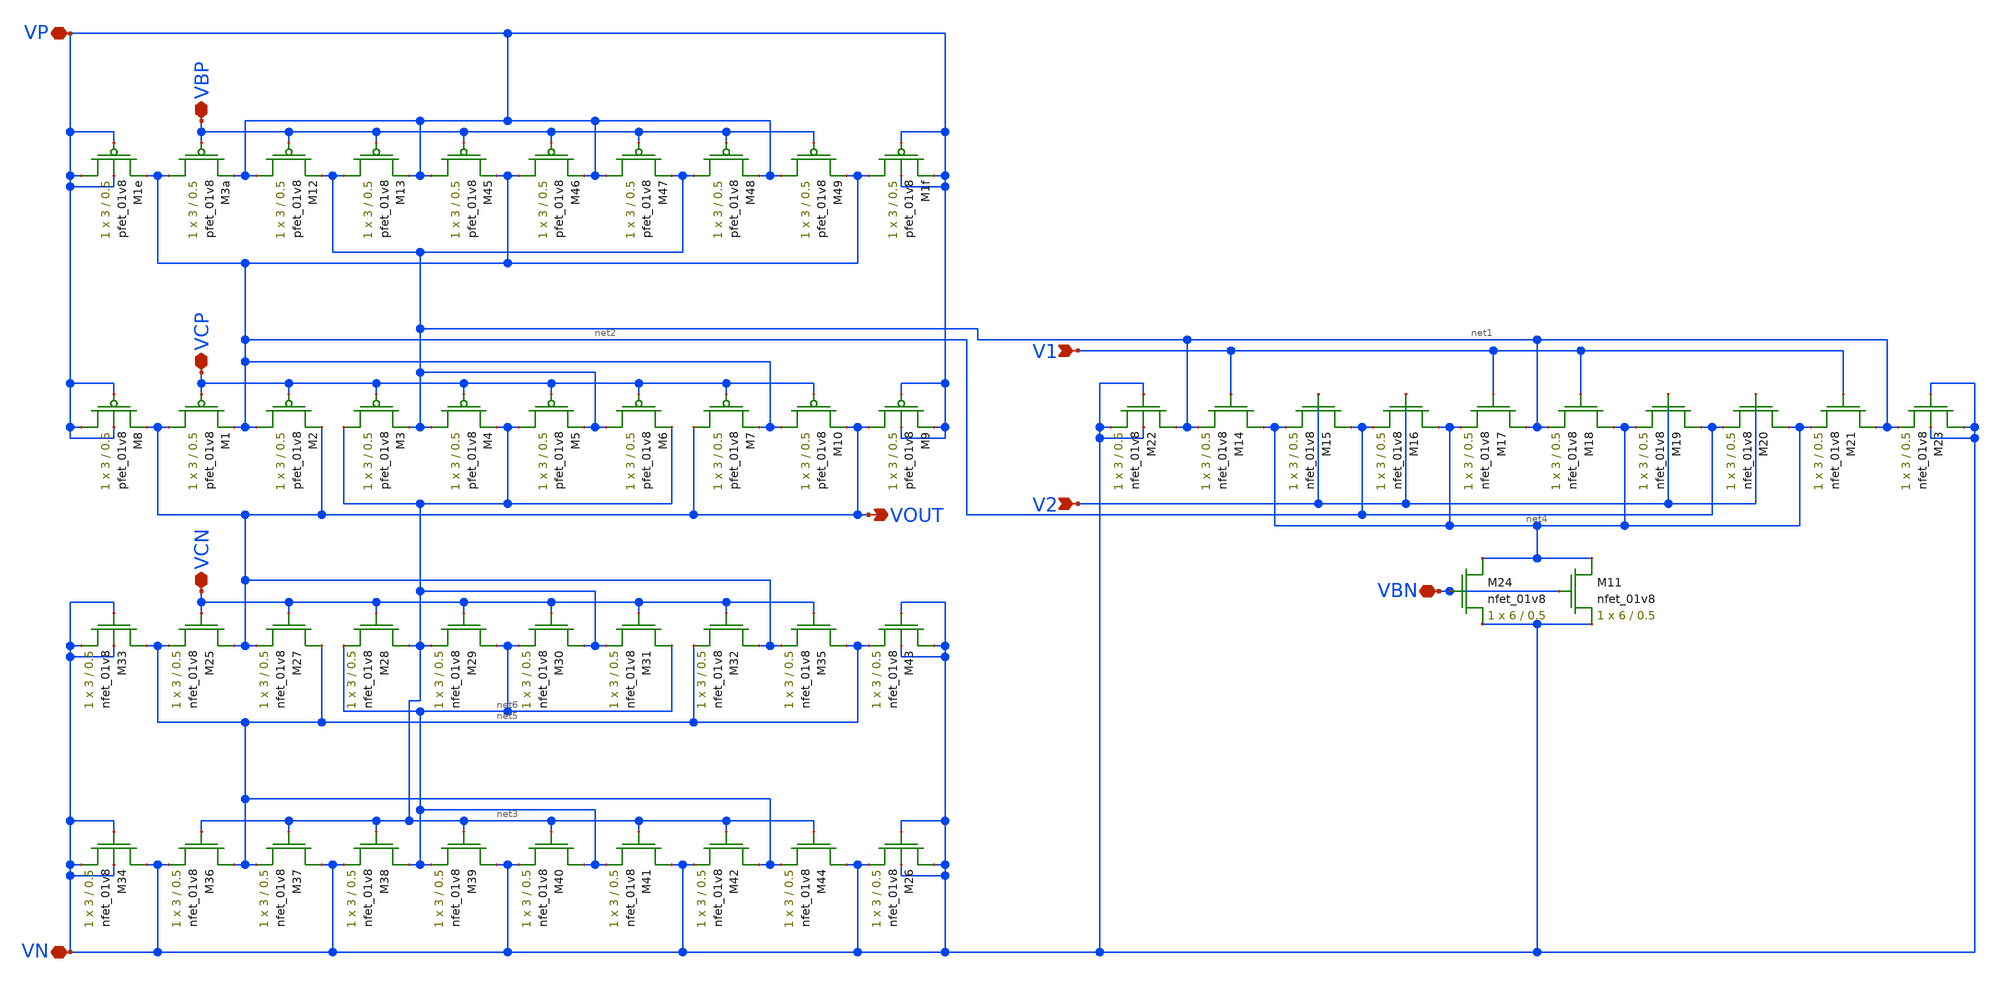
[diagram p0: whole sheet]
** sch_path: differential_amplifier/schematics/folded_cascode_differential_amplifier.sch
**.subckt folded_cascode_differential_amplifier VBP VCP V1 V2 VBN VCN VP VN VOUT
*.iopin VBP
*.iopin VCP
*.ipin V1
*.ipin V2
*.iopin VBN
*.iopin VCN
*.iopin VP
*.iopin VN
*.opin VOUT
XM3a net2 VBP VP VP sky130_fd_pr__pfet_01v8 L=0.5 W=3 nf=1 ad='int((nf+1)/2) * W/nf * 0.29' as='int((nf+2)/2) * W/nf * 0.29'
+ pd='2*int((nf+1)/2) * (W/nf + 0.29)' ps='2*int((nf+2)/2) * (W/nf + 0.29)' nrd='0.29 / W' nrs='0.29 / W'
+ sa=0 sb=0 sd=0 mult=1 m=1
XM1e VP VP net2 VP sky130_fd_pr__pfet_01v8 L=0.5 W=3 nf=1 ad='int((nf+1)/2) * W/nf * 0.29' as='int((nf+2)/2) * W/nf * 0.29'
+ pd='2*int((nf+1)/2) * (W/nf + 0.29)' ps='2*int((nf+2)/2) * (W/nf + 0.29)' nrd='0.29 / W' nrs='0.29 / W'
+ sa=0 sb=0 sd=0 mult=1 m=1
XM1f net2 VP VP VP sky130_fd_pr__pfet_01v8 L=0.5 W=3 nf=1 ad='int((nf+1)/2) * W/nf * 0.29' as='int((nf+2)/2) * W/nf * 0.29'
+ pd='2*int((nf+1)/2) * (W/nf + 0.29)' ps='2*int((nf+2)/2) * (W/nf + 0.29)' nrd='0.29 / W' nrs='0.29 / W'
+ sa=0 sb=0 sd=0 mult=1 m=1
XM8 VP VP VOUT VP sky130_fd_pr__pfet_01v8 L=0.5 W=3 nf=1 ad='int((nf+1)/2) * W/nf * 0.29' as='int((nf+2)/2) * W/nf * 0.29'
+ pd='2*int((nf+1)/2) * (W/nf + 0.29)' ps='2*int((nf+2)/2) * (W/nf + 0.29)' nrd='0.29 / W' nrs='0.29 / W'
+ sa=0 sb=0 sd=0 mult=1 m=1
XM9 VOUT VP VP VP sky130_fd_pr__pfet_01v8 L=0.5 W=3 nf=1 ad='int((nf+1)/2) * W/nf * 0.29' as='int((nf+2)/2) * W/nf * 0.29'
+ pd='2*int((nf+1)/2) * (W/nf + 0.29)' ps='2*int((nf+2)/2) * (W/nf + 0.29)' nrd='0.29 / W' nrs='0.29 / W'
+ sa=0 sb=0 sd=0 mult=1 m=1
XM22 net1 VN VN VN sky130_fd_pr__nfet_01v8 L=0.5 W=3 nf=1 ad='int((nf+1)/2) * W/nf * 0.29' as='int((nf+2)/2) * W/nf * 0.29'
+ pd='2*int((nf+1)/2) * (W/nf + 0.29)' ps='2*int((nf+2)/2) * (W/nf + 0.29)' nrd='0.29 / W' nrs='0.29 / W'
+ sa=0 sb=0 sd=0 mult=1 m=1
XM23 VN VN net1 VN sky130_fd_pr__nfet_01v8 L=0.5 W=3 nf=1 ad='int((nf+1)/2) * W/nf * 0.29' as='int((nf+2)/2) * W/nf * 0.29'
+ pd='2*int((nf+1)/2) * (W/nf + 0.29)' ps='2*int((nf+2)/2) * (W/nf + 0.29)' nrd='0.29 / W' nrs='0.29 / W'
+ sa=0 sb=0 sd=0 mult=1 m=1
XM24 net4 VBN VN VN sky130_fd_pr__nfet_01v8 L=0.5 W=6 nf=1 ad='int((nf+1)/2) * W/nf * 0.29' as='int((nf+2)/2) * W/nf * 0.29'
+ pd='2*int((nf+1)/2) * (W/nf + 0.29)' ps='2*int((nf+2)/2) * (W/nf + 0.29)' nrd='0.29 / W' nrs='0.29 / W'
+ sa=0 sb=0 sd=0 mult=1 m=1
XM25 VOUT VCN net5 VN sky130_fd_pr__nfet_01v8 L=0.5 W=3 nf=1 ad='int((nf+1)/2) * W/nf * 0.29' as='int((nf+2)/2) * W/nf * 0.29'
+ pd='2*int((nf+1)/2) * (W/nf + 0.29)' ps='2*int((nf+2)/2) * (W/nf + 0.29)' nrd='0.29 / W' nrs='0.29 / W'
+ sa=0 sb=0 sd=0 mult=1 m=1
XM33 net5 VN VN VN sky130_fd_pr__nfet_01v8 L=0.5 W=3 nf=1 ad='int((nf+1)/2) * W/nf * 0.29' as='int((nf+2)/2) * W/nf * 0.29'
+ pd='2*int((nf+1)/2) * (W/nf + 0.29)' ps='2*int((nf+2)/2) * (W/nf + 0.29)' nrd='0.29 / W' nrs='0.29 / W'
+ sa=0 sb=0 sd=0 mult=1 m=1
XM34 VN VN VN VN sky130_fd_pr__nfet_01v8 L=0.5 W=3 nf=1 ad='int((nf+1)/2) * W/nf * 0.29' as='int((nf+2)/2) * W/nf * 0.29'
+ pd='2*int((nf+1)/2) * (W/nf + 0.29)' ps='2*int((nf+2)/2) * (W/nf + 0.29)' nrd='0.29 / W' nrs='0.29 / W'
+ sa=0 sb=0 sd=0 mult=1 m=1
XM43 VN VN net5 VN sky130_fd_pr__nfet_01v8 L=0.5 W=3 nf=1 ad='int((nf+1)/2) * W/nf * 0.29' as='int((nf+2)/2) * W/nf * 0.29'
+ pd='2*int((nf+1)/2) * (W/nf + 0.29)' ps='2*int((nf+2)/2) * (W/nf + 0.29)' nrd='0.29 / W' nrs='0.29 / W'
+ sa=0 sb=0 sd=0 mult=1 m=1
XM11 net4 VBN VN VN sky130_fd_pr__nfet_01v8 L=0.5 W=6 nf=1 ad='int((nf+1)/2) * W/nf * 0.29' as='int((nf+2)/2) * W/nf * 0.29'
+ pd='2*int((nf+1)/2) * (W/nf + 0.29)' ps='2*int((nf+2)/2) * (W/nf + 0.29)' nrd='0.29 / W' nrs='0.29 / W'
+ sa=0 sb=0 sd=0 mult=1 m=1
XM12 VP VBP net1 VP sky130_fd_pr__pfet_01v8 L=0.5 W=3 nf=1 ad='int((nf+1)/2) * W/nf * 0.29' as='int((nf+2)/2) * W/nf * 0.29'
+ pd='2*int((nf+1)/2) * (W/nf + 0.29)' ps='2*int((nf+2)/2) * (W/nf + 0.29)' nrd='0.29 / W' nrs='0.29 / W'
+ sa=0 sb=0 sd=0 mult=1 m=1
XM13 net1 VBP VP VP sky130_fd_pr__pfet_01v8 L=0.5 W=3 nf=1 ad='int((nf+1)/2) * W/nf * 0.29' as='int((nf+2)/2) * W/nf * 0.29'
+ pd='2*int((nf+1)/2) * (W/nf + 0.29)' ps='2*int((nf+2)/2) * (W/nf + 0.29)' nrd='0.29 / W' nrs='0.29 / W'
+ sa=0 sb=0 sd=0 mult=1 m=1
XM45 VP VBP net2 VP sky130_fd_pr__pfet_01v8 L=0.5 W=3 nf=1 ad='int((nf+1)/2) * W/nf * 0.29' as='int((nf+2)/2) * W/nf * 0.29'
+ pd='2*int((nf+1)/2) * (W/nf + 0.29)' ps='2*int((nf+2)/2) * (W/nf + 0.29)' nrd='0.29 / W' nrs='0.29 / W'
+ sa=0 sb=0 sd=0 mult=1 m=1
XM46 net2 VBP VP VP sky130_fd_pr__pfet_01v8 L=0.5 W=3 nf=1 ad='int((nf+1)/2) * W/nf * 0.29' as='int((nf+2)/2) * W/nf * 0.29'
+ pd='2*int((nf+1)/2) * (W/nf + 0.29)' ps='2*int((nf+2)/2) * (W/nf + 0.29)' nrd='0.29 / W' nrs='0.29 / W'
+ sa=0 sb=0 sd=0 mult=1 m=1
XM47 VP VBP net1 VP sky130_fd_pr__pfet_01v8 L=0.5 W=3 nf=1 ad='int((nf+1)/2) * W/nf * 0.29' as='int((nf+2)/2) * W/nf * 0.29'
+ pd='2*int((nf+1)/2) * (W/nf + 0.29)' ps='2*int((nf+2)/2) * (W/nf + 0.29)' nrd='0.29 / W' nrs='0.29 / W'
+ sa=0 sb=0 sd=0 mult=1 m=1
XM48 net1 VBP VP VP sky130_fd_pr__pfet_01v8 L=0.5 W=3 nf=1 ad='int((nf+1)/2) * W/nf * 0.29' as='int((nf+2)/2) * W/nf * 0.29'
+ pd='2*int((nf+1)/2) * (W/nf + 0.29)' ps='2*int((nf+2)/2) * (W/nf + 0.29)' nrd='0.29 / W' nrs='0.29 / W'
+ sa=0 sb=0 sd=0 mult=1 m=1
XM49 VP VBP net2 VP sky130_fd_pr__pfet_01v8 L=0.5 W=3 nf=1 ad='int((nf+1)/2) * W/nf * 0.29' as='int((nf+2)/2) * W/nf * 0.29'
+ pd='2*int((nf+1)/2) * (W/nf + 0.29)' ps='2*int((nf+2)/2) * (W/nf + 0.29)' nrd='0.29 / W' nrs='0.29 / W'
+ sa=0 sb=0 sd=0 mult=1 m=1
XM1 VOUT VCP net2 VP sky130_fd_pr__pfet_01v8 L=0.5 W=3 nf=1 ad='int((nf+1)/2) * W/nf * 0.29' as='int((nf+2)/2) * W/nf * 0.29'
+ pd='2*int((nf+1)/2) * (W/nf + 0.29)' ps='2*int((nf+2)/2) * (W/nf + 0.29)' nrd='0.29 / W' nrs='0.29 / W'
+ sa=0 sb=0 sd=0 mult=1 m=1
XM2 net2 VCP VOUT VP sky130_fd_pr__pfet_01v8 L=0.5 W=3 nf=1 ad='int((nf+1)/2) * W/nf * 0.29' as='int((nf+2)/2) * W/nf * 0.29'
+ pd='2*int((nf+1)/2) * (W/nf + 0.29)' ps='2*int((nf+2)/2) * (W/nf + 0.29)' nrd='0.29 / W' nrs='0.29 / W'
+ sa=0 sb=0 sd=0 mult=1 m=1
XM3 net3 VCP net1 VP sky130_fd_pr__pfet_01v8 L=0.5 W=3 nf=1 ad='int((nf+1)/2) * W/nf * 0.29' as='int((nf+2)/2) * W/nf * 0.29'
+ pd='2*int((nf+1)/2) * (W/nf + 0.29)' ps='2*int((nf+2)/2) * (W/nf + 0.29)' nrd='0.29 / W' nrs='0.29 / W'
+ sa=0 sb=0 sd=0 mult=1 m=1
XM4 net1 VCP net3 VP sky130_fd_pr__pfet_01v8 L=0.5 W=3 nf=1 ad='int((nf+1)/2) * W/nf * 0.29' as='int((nf+2)/2) * W/nf * 0.29'
+ pd='2*int((nf+1)/2) * (W/nf + 0.29)' ps='2*int((nf+2)/2) * (W/nf + 0.29)' nrd='0.29 / W' nrs='0.29 / W'
+ sa=0 sb=0 sd=0 mult=1 m=1
XM5 net3 VCP net1 VP sky130_fd_pr__pfet_01v8 L=0.5 W=3 nf=1 ad='int((nf+1)/2) * W/nf * 0.29' as='int((nf+2)/2) * W/nf * 0.29'
+ pd='2*int((nf+1)/2) * (W/nf + 0.29)' ps='2*int((nf+2)/2) * (W/nf + 0.29)' nrd='0.29 / W' nrs='0.29 / W'
+ sa=0 sb=0 sd=0 mult=1 m=1
XM6 net1 VCP net3 VP sky130_fd_pr__pfet_01v8 L=0.5 W=3 nf=1 ad='int((nf+1)/2) * W/nf * 0.29' as='int((nf+2)/2) * W/nf * 0.29'
+ pd='2*int((nf+1)/2) * (W/nf + 0.29)' ps='2*int((nf+2)/2) * (W/nf + 0.29)' nrd='0.29 / W' nrs='0.29 / W'
+ sa=0 sb=0 sd=0 mult=1 m=1
XM7 VOUT VCP net2 VP sky130_fd_pr__pfet_01v8 L=0.5 W=3 nf=1 ad='int((nf+1)/2) * W/nf * 0.29' as='int((nf+2)/2) * W/nf * 0.29'
+ pd='2*int((nf+1)/2) * (W/nf + 0.29)' ps='2*int((nf+2)/2) * (W/nf + 0.29)' nrd='0.29 / W' nrs='0.29 / W'
+ sa=0 sb=0 sd=0 mult=1 m=1
XM10 net2 VCP VOUT VP sky130_fd_pr__pfet_01v8 L=0.5 W=3 nf=1 ad='int((nf+1)/2) * W/nf * 0.29' as='int((nf+2)/2) * W/nf * 0.29'
+ pd='2*int((nf+1)/2) * (W/nf + 0.29)' ps='2*int((nf+2)/2) * (W/nf + 0.29)' nrd='0.29 / W' nrs='0.29 / W'
+ sa=0 sb=0 sd=0 mult=1 m=1
XM26 VN VN VN VN sky130_fd_pr__nfet_01v8 L=0.5 W=3 nf=1 ad='int((nf+1)/2) * W/nf * 0.29' as='int((nf+2)/2) * W/nf * 0.29'
+ pd='2*int((nf+1)/2) * (W/nf + 0.29)' ps='2*int((nf+2)/2) * (W/nf + 0.29)' nrd='0.29 / W' nrs='0.29 / W'
+ sa=0 sb=0 sd=0 mult=1 m=1
XM27 net5 VCN VOUT VN sky130_fd_pr__nfet_01v8 L=0.5 W=3 nf=1 ad='int((nf+1)/2) * W/nf * 0.29' as='int((nf+2)/2) * W/nf * 0.29'
+ pd='2*int((nf+1)/2) * (W/nf + 0.29)' ps='2*int((nf+2)/2) * (W/nf + 0.29)' nrd='0.29 / W' nrs='0.29 / W'
+ sa=0 sb=0 sd=0 mult=1 m=1
XM28 net3 VCN net6 VN sky130_fd_pr__nfet_01v8 L=0.5 W=3 nf=1 ad='int((nf+1)/2) * W/nf * 0.29' as='int((nf+2)/2) * W/nf * 0.29'
+ pd='2*int((nf+1)/2) * (W/nf + 0.29)' ps='2*int((nf+2)/2) * (W/nf + 0.29)' nrd='0.29 / W' nrs='0.29 / W'
+ sa=0 sb=0 sd=0 mult=1 m=1
XM29 net6 VCN net3 VN sky130_fd_pr__nfet_01v8 L=0.5 W=3 nf=1 ad='int((nf+1)/2) * W/nf * 0.29' as='int((nf+2)/2) * W/nf * 0.29'
+ pd='2*int((nf+1)/2) * (W/nf + 0.29)' ps='2*int((nf+2)/2) * (W/nf + 0.29)' nrd='0.29 / W' nrs='0.29 / W'
+ sa=0 sb=0 sd=0 mult=1 m=1
XM30 net3 VCN net6 VN sky130_fd_pr__nfet_01v8 L=0.5 W=3 nf=1 ad='int((nf+1)/2) * W/nf * 0.29' as='int((nf+2)/2) * W/nf * 0.29'
+ pd='2*int((nf+1)/2) * (W/nf + 0.29)' ps='2*int((nf+2)/2) * (W/nf + 0.29)' nrd='0.29 / W' nrs='0.29 / W'
+ sa=0 sb=0 sd=0 mult=1 m=1
XM31 net6 VCN net3 VN sky130_fd_pr__nfet_01v8 L=0.5 W=3 nf=1 ad='int((nf+1)/2) * W/nf * 0.29' as='int((nf+2)/2) * W/nf * 0.29'
+ pd='2*int((nf+1)/2) * (W/nf + 0.29)' ps='2*int((nf+2)/2) * (W/nf + 0.29)' nrd='0.29 / W' nrs='0.29 / W'
+ sa=0 sb=0 sd=0 mult=1 m=1
XM32 VOUT VCN net5 VN sky130_fd_pr__nfet_01v8 L=0.5 W=3 nf=1 ad='int((nf+1)/2) * W/nf * 0.29' as='int((nf+2)/2) * W/nf * 0.29'
+ pd='2*int((nf+1)/2) * (W/nf + 0.29)' ps='2*int((nf+2)/2) * (W/nf + 0.29)' nrd='0.29 / W' nrs='0.29 / W'
+ sa=0 sb=0 sd=0 mult=1 m=1
XM35 net5 VCN VOUT VN sky130_fd_pr__nfet_01v8 L=0.5 W=3 nf=1 ad='int((nf+1)/2) * W/nf * 0.29' as='int((nf+2)/2) * W/nf * 0.29'
+ pd='2*int((nf+1)/2) * (W/nf + 0.29)' ps='2*int((nf+2)/2) * (W/nf + 0.29)' nrd='0.29 / W' nrs='0.29 / W'
+ sa=0 sb=0 sd=0 mult=1 m=1
XM36 net5 net3 VN VN sky130_fd_pr__nfet_01v8 L=0.5 W=3 nf=1 ad='int((nf+1)/2) * W/nf * 0.29' as='int((nf+2)/2) * W/nf * 0.29'
+ pd='2*int((nf+1)/2) * (W/nf + 0.29)' ps='2*int((nf+2)/2) * (W/nf + 0.29)' nrd='0.29 / W' nrs='0.29 / W'
+ sa=0 sb=0 sd=0 mult=1 m=1
XM37 VN net3 net5 VN sky130_fd_pr__nfet_01v8 L=0.5 W=3 nf=1 ad='int((nf+1)/2) * W/nf * 0.29' as='int((nf+2)/2) * W/nf * 0.29'
+ pd='2*int((nf+1)/2) * (W/nf + 0.29)' ps='2*int((nf+2)/2) * (W/nf + 0.29)' nrd='0.29 / W' nrs='0.29 / W'
+ sa=0 sb=0 sd=0 mult=1 m=1
XM38 net6 net3 VN VN sky130_fd_pr__nfet_01v8 L=0.5 W=3 nf=1 ad='int((nf+1)/2) * W/nf * 0.29' as='int((nf+2)/2) * W/nf * 0.29'
+ pd='2*int((nf+1)/2) * (W/nf + 0.29)' ps='2*int((nf+2)/2) * (W/nf + 0.29)' nrd='0.29 / W' nrs='0.29 / W'
+ sa=0 sb=0 sd=0 mult=1 m=1
XM39 VN net3 net6 VN sky130_fd_pr__nfet_01v8 L=0.5 W=3 nf=1 ad='int((nf+1)/2) * W/nf * 0.29' as='int((nf+2)/2) * W/nf * 0.29'
+ pd='2*int((nf+1)/2) * (W/nf + 0.29)' ps='2*int((nf+2)/2) * (W/nf + 0.29)' nrd='0.29 / W' nrs='0.29 / W'
+ sa=0 sb=0 sd=0 mult=1 m=1
XM40 net6 net3 VN VN sky130_fd_pr__nfet_01v8 L=0.5 W=3 nf=1 ad='int((nf+1)/2) * W/nf * 0.29' as='int((nf+2)/2) * W/nf * 0.29'
+ pd='2*int((nf+1)/2) * (W/nf + 0.29)' ps='2*int((nf+2)/2) * (W/nf + 0.29)' nrd='0.29 / W' nrs='0.29 / W'
+ sa=0 sb=0 sd=0 mult=1 m=1
XM41 VN net3 net6 VN sky130_fd_pr__nfet_01v8 L=0.5 W=3 nf=1 ad='int((nf+1)/2) * W/nf * 0.29' as='int((nf+2)/2) * W/nf * 0.29'
+ pd='2*int((nf+1)/2) * (W/nf + 0.29)' ps='2*int((nf+2)/2) * (W/nf + 0.29)' nrd='0.29 / W' nrs='0.29 / W'
+ sa=0 sb=0 sd=0 mult=1 m=1
XM42 net5 net3 VN VN sky130_fd_pr__nfet_01v8 L=0.5 W=3 nf=1 ad='int((nf+1)/2) * W/nf * 0.29' as='int((nf+2)/2) * W/nf * 0.29'
+ pd='2*int((nf+1)/2) * (W/nf + 0.29)' ps='2*int((nf+2)/2) * (W/nf + 0.29)' nrd='0.29 / W' nrs='0.29 / W'
+ sa=0 sb=0 sd=0 mult=1 m=1
XM44 VN net3 net5 VN sky130_fd_pr__nfet_01v8 L=0.5 W=3 nf=1 ad='int((nf+1)/2) * W/nf * 0.29' as='int((nf+2)/2) * W/nf * 0.29'
+ pd='2*int((nf+1)/2) * (W/nf + 0.29)' ps='2*int((nf+2)/2) * (W/nf + 0.29)' nrd='0.29 / W' nrs='0.29 / W'
+ sa=0 sb=0 sd=0 mult=1 m=1
XM14 net4 V1 net1 VN sky130_fd_pr__nfet_01v8 L=0.5 W=3 nf=1 ad='int((nf+1)/2) * W/nf * 0.29' as='int((nf+2)/2) * W/nf * 0.29'
+ pd='2*int((nf+1)/2) * (W/nf + 0.29)' ps='2*int((nf+2)/2) * (W/nf + 0.29)' nrd='0.29 / W' nrs='0.29 / W'
+ sa=0 sb=0 sd=0 mult=1 m=1
XM15 net2 V2 net4 VN sky130_fd_pr__nfet_01v8 L=0.5 W=3 nf=1 ad='int((nf+1)/2) * W/nf * 0.29' as='int((nf+2)/2) * W/nf * 0.29'
+ pd='2*int((nf+1)/2) * (W/nf + 0.29)' ps='2*int((nf+2)/2) * (W/nf + 0.29)' nrd='0.29 / W' nrs='0.29 / W'
+ sa=0 sb=0 sd=0 mult=1 m=1
XM16 net4 V2 net2 VN sky130_fd_pr__nfet_01v8 L=0.5 W=3 nf=1 ad='int((nf+1)/2) * W/nf * 0.29' as='int((nf+2)/2) * W/nf * 0.29'
+ pd='2*int((nf+1)/2) * (W/nf + 0.29)' ps='2*int((nf+2)/2) * (W/nf + 0.29)' nrd='0.29 / W' nrs='0.29 / W'
+ sa=0 sb=0 sd=0 mult=1 m=1
XM17 net1 V1 net4 VN sky130_fd_pr__nfet_01v8 L=0.5 W=3 nf=1 ad='int((nf+1)/2) * W/nf * 0.29' as='int((nf+2)/2) * W/nf * 0.29'
+ pd='2*int((nf+1)/2) * (W/nf + 0.29)' ps='2*int((nf+2)/2) * (W/nf + 0.29)' nrd='0.29 / W' nrs='0.29 / W'
+ sa=0 sb=0 sd=0 mult=1 m=1
XM18 net4 V1 net1 VN sky130_fd_pr__nfet_01v8 L=0.5 W=3 nf=1 ad='int((nf+1)/2) * W/nf * 0.29' as='int((nf+2)/2) * W/nf * 0.29'
+ pd='2*int((nf+1)/2) * (W/nf + 0.29)' ps='2*int((nf+2)/2) * (W/nf + 0.29)' nrd='0.29 / W' nrs='0.29 / W'
+ sa=0 sb=0 sd=0 mult=1 m=1
XM19 net2 V2 net4 VN sky130_fd_pr__nfet_01v8 L=0.5 W=3 nf=1 ad='int((nf+1)/2) * W/nf * 0.29' as='int((nf+2)/2) * W/nf * 0.29'
+ pd='2*int((nf+1)/2) * (W/nf + 0.29)' ps='2*int((nf+2)/2) * (W/nf + 0.29)' nrd='0.29 / W' nrs='0.29 / W'
+ sa=0 sb=0 sd=0 mult=1 m=1
XM20 net4 V2 net2 VN sky130_fd_pr__nfet_01v8 L=0.5 W=3 nf=1 ad='int((nf+1)/2) * W/nf * 0.29' as='int((nf+2)/2) * W/nf * 0.29'
+ pd='2*int((nf+1)/2) * (W/nf + 0.29)' ps='2*int((nf+2)/2) * (W/nf + 0.29)' nrd='0.29 / W' nrs='0.29 / W'
+ sa=0 sb=0 sd=0 mult=1 m=1
XM21 net1 V1 net4 VN sky130_fd_pr__nfet_01v8 L=0.5 W=3 nf=1 ad='int((nf+1)/2) * W/nf * 0.29' as='int((nf+2)/2) * W/nf * 0.29'
+ pd='2*int((nf+1)/2) * (W/nf + 0.29)' ps='2*int((nf+2)/2) * (W/nf + 0.29)' nrd='0.29 / W' nrs='0.29 / W'
+ sa=0 sb=0 sd=0 mult=1 m=1
**.ends
.end
